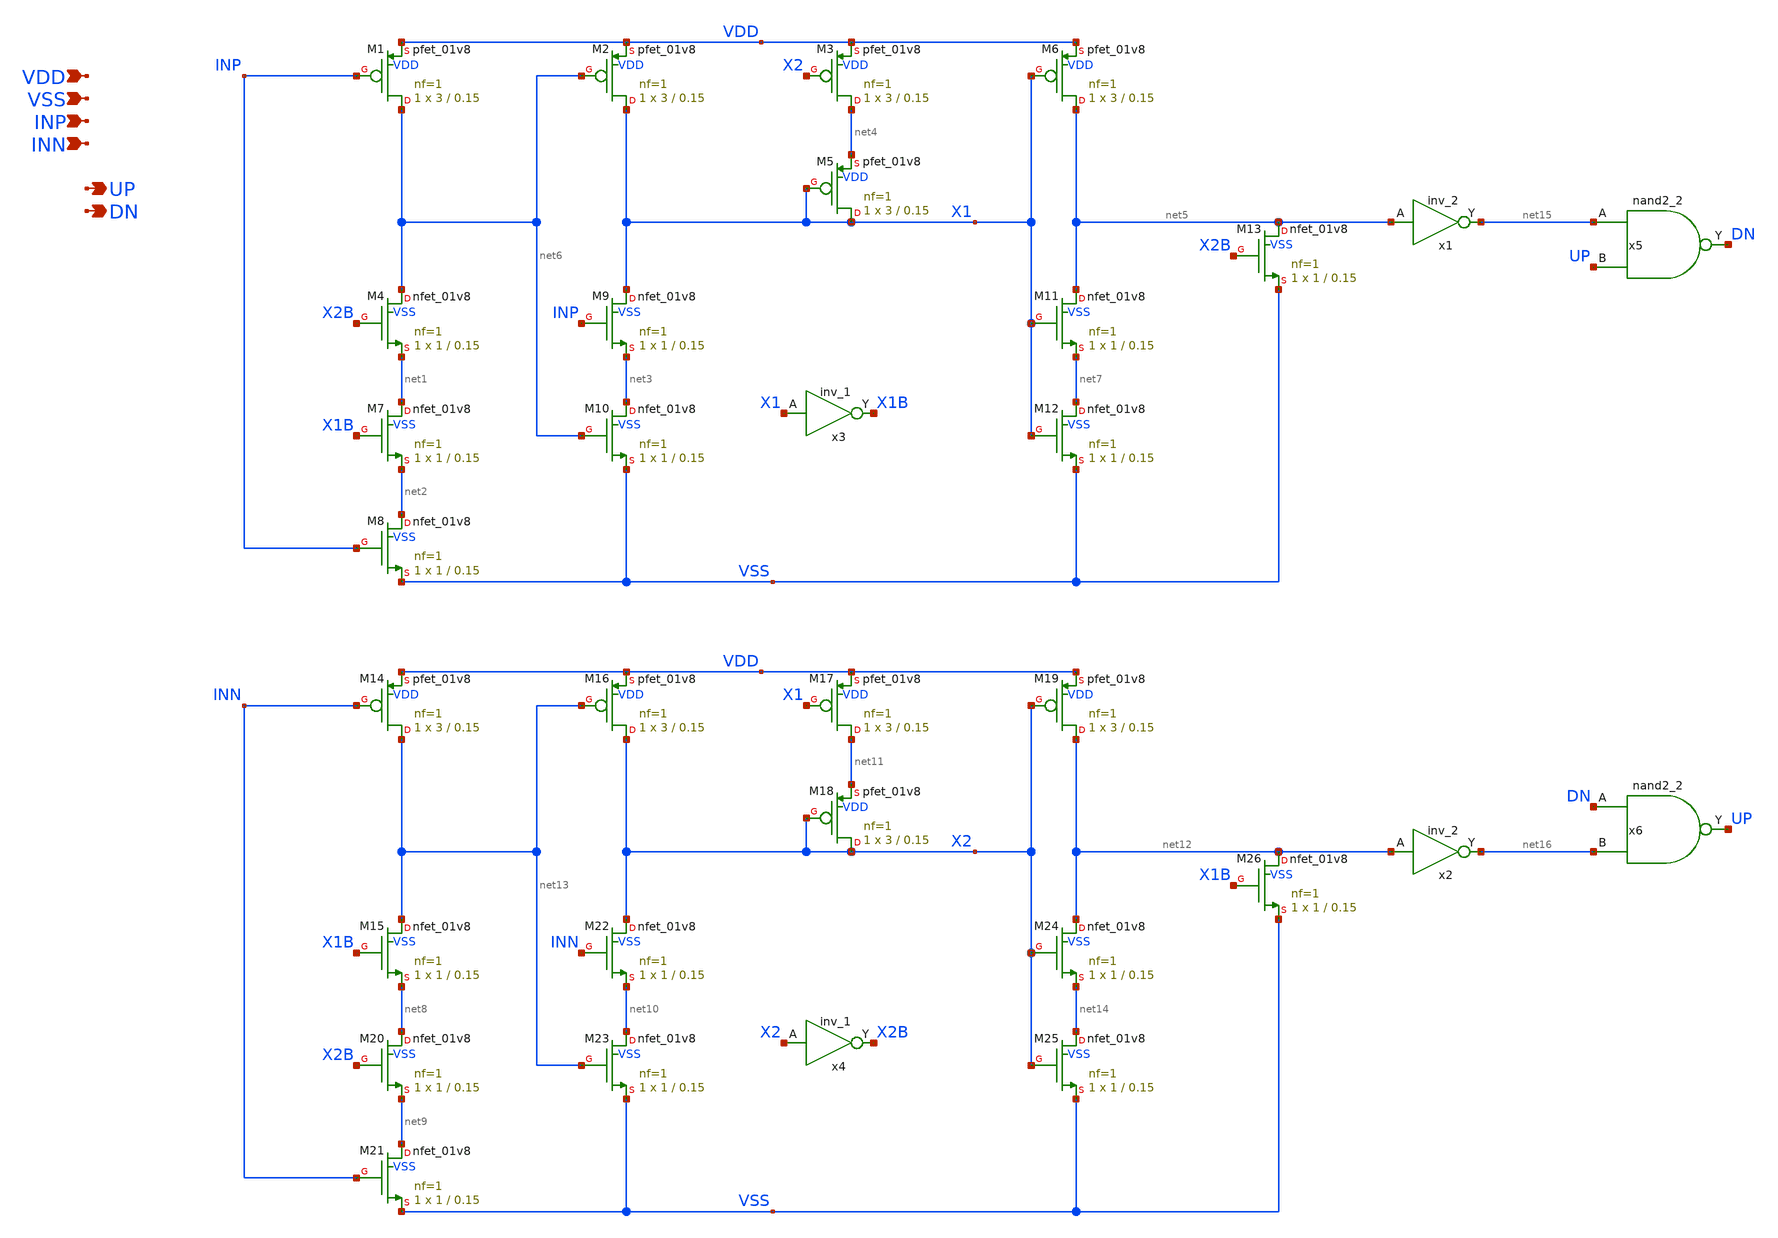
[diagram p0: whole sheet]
** sch_path: xschem/pfd.sch
**.subckt pfd VDD VSS INP INN UP DN
*.ipin VDD
*.ipin VSS
*.ipin INP
*.ipin INN
*.opin UP
*.opin DN
XM1 net6 INP VDD VDD sky130_fd_pr__pfet_01v8 L=0.15 W=3 nf=1 ad='int((nf+1)/2) * W/nf * 0.29' as='int((nf+2)/2) * W/nf * 0.29'
+ pd='2*int((nf+1)/2) * (W/nf + 0.29)' ps='2*int((nf+2)/2) * (W/nf + 0.29)' nrd='0.29 / W' nrs='0.29 / W'
+ sa=0 sb=0 sd=0 mult=1 m=1
XM4 net6 X2B net1 VSS sky130_fd_pr__nfet_01v8 L=0.15 W=1 nf=1 ad='int((nf+1)/2) * W/nf * 0.29' as='int((nf+2)/2) * W/nf * 0.29'
+ pd='2*int((nf+1)/2) * (W/nf + 0.29)' ps='2*int((nf+2)/2) * (W/nf + 0.29)' nrd='0.29 / W' nrs='0.29 / W'
+ sa=0 sb=0 sd=0 mult=1 m=1
XM2 X1 net6 VDD VDD sky130_fd_pr__pfet_01v8 L=0.15 W=3 nf=1 ad='int((nf+1)/2) * W/nf * 0.29' as='int((nf+2)/2) * W/nf * 0.29'
+ pd='2*int((nf+1)/2) * (W/nf + 0.29)' ps='2*int((nf+2)/2) * (W/nf + 0.29)' nrd='0.29 / W' nrs='0.29 / W'
+ sa=0 sb=0 sd=0 mult=1 m=1
XM3 net4 X2 VDD VDD sky130_fd_pr__pfet_01v8 L=0.15 W=3 nf=1 ad='int((nf+1)/2) * W/nf * 0.29' as='int((nf+2)/2) * W/nf * 0.29'
+ pd='2*int((nf+1)/2) * (W/nf + 0.29)' ps='2*int((nf+2)/2) * (W/nf + 0.29)' nrd='0.29 / W' nrs='0.29 / W'
+ sa=0 sb=0 sd=0 mult=1 m=1
XM5 X1 X1 net4 VDD sky130_fd_pr__pfet_01v8 L=0.15 W=3 nf=1 ad='int((nf+1)/2) * W/nf * 0.29' as='int((nf+2)/2) * W/nf * 0.29'
+ pd='2*int((nf+1)/2) * (W/nf + 0.29)' ps='2*int((nf+2)/2) * (W/nf + 0.29)' nrd='0.29 / W' nrs='0.29 / W'
+ sa=0 sb=0 sd=0 mult=1 m=1
XM6 net5 X1 VDD VDD sky130_fd_pr__pfet_01v8 L=0.15 W=3 nf=1 ad='int((nf+1)/2) * W/nf * 0.29' as='int((nf+2)/2) * W/nf * 0.29'
+ pd='2*int((nf+1)/2) * (W/nf + 0.29)' ps='2*int((nf+2)/2) * (W/nf + 0.29)' nrd='0.29 / W' nrs='0.29 / W'
+ sa=0 sb=0 sd=0 mult=1 m=1
XM7 net1 X1B net2 VSS sky130_fd_pr__nfet_01v8 L=0.15 W=1 nf=1 ad='int((nf+1)/2) * W/nf * 0.29' as='int((nf+2)/2) * W/nf * 0.29'
+ pd='2*int((nf+1)/2) * (W/nf + 0.29)' ps='2*int((nf+2)/2) * (W/nf + 0.29)' nrd='0.29 / W' nrs='0.29 / W'
+ sa=0 sb=0 sd=0 mult=1 m=1
XM8 net2 INP VSS VSS sky130_fd_pr__nfet_01v8 L=0.15 W=1 nf=1 ad='int((nf+1)/2) * W/nf * 0.29' as='int((nf+2)/2) * W/nf * 0.29'
+ pd='2*int((nf+1)/2) * (W/nf + 0.29)' ps='2*int((nf+2)/2) * (W/nf + 0.29)' nrd='0.29 / W' nrs='0.29 / W'
+ sa=0 sb=0 sd=0 mult=1 m=1
XM9 X1 INP net3 VSS sky130_fd_pr__nfet_01v8 L=0.15 W=1 nf=1 ad='int((nf+1)/2) * W/nf * 0.29' as='int((nf+2)/2) * W/nf * 0.29'
+ pd='2*int((nf+1)/2) * (W/nf + 0.29)' ps='2*int((nf+2)/2) * (W/nf + 0.29)' nrd='0.29 / W' nrs='0.29 / W'
+ sa=0 sb=0 sd=0 mult=1 m=1
XM10 net3 net6 VSS VSS sky130_fd_pr__nfet_01v8 L=0.15 W=1 nf=1 ad='int((nf+1)/2) * W/nf * 0.29' as='int((nf+2)/2) * W/nf * 0.29'
+ pd='2*int((nf+1)/2) * (W/nf + 0.29)' ps='2*int((nf+2)/2) * (W/nf + 0.29)' nrd='0.29 / W' nrs='0.29 / W'
+ sa=0 sb=0 sd=0 mult=1 m=1
XM11 net5 X1 net7 VSS sky130_fd_pr__nfet_01v8 L=0.15 W=1 nf=1 ad='int((nf+1)/2) * W/nf * 0.29' as='int((nf+2)/2) * W/nf * 0.29'
+ pd='2*int((nf+1)/2) * (W/nf + 0.29)' ps='2*int((nf+2)/2) * (W/nf + 0.29)' nrd='0.29 / W' nrs='0.29 / W'
+ sa=0 sb=0 sd=0 mult=1 m=1
XM12 net7 X1 VSS VSS sky130_fd_pr__nfet_01v8 L=0.15 W=1 nf=1 ad='int((nf+1)/2) * W/nf * 0.29' as='int((nf+2)/2) * W/nf * 0.29'
+ pd='2*int((nf+1)/2) * (W/nf + 0.29)' ps='2*int((nf+2)/2) * (W/nf + 0.29)' nrd='0.29 / W' nrs='0.29 / W'
+ sa=0 sb=0 sd=0 mult=1 m=1
XM13 net5 X2B VSS VSS sky130_fd_pr__nfet_01v8 L=0.15 W=1 nf=1 ad='int((nf+1)/2) * W/nf * 0.29' as='int((nf+2)/2) * W/nf * 0.29'
+ pd='2*int((nf+1)/2) * (W/nf + 0.29)' ps='2*int((nf+2)/2) * (W/nf + 0.29)' nrd='0.29 / W' nrs='0.29 / W'
+ sa=0 sb=0 sd=0 mult=1 m=1
XM14 net13 INN VDD VDD sky130_fd_pr__pfet_01v8 L=0.15 W=3 nf=1 ad='int((nf+1)/2) * W/nf * 0.29' as='int((nf+2)/2) * W/nf * 0.29'
+ pd='2*int((nf+1)/2) * (W/nf + 0.29)' ps='2*int((nf+2)/2) * (W/nf + 0.29)' nrd='0.29 / W' nrs='0.29 / W'
+ sa=0 sb=0 sd=0 mult=1 m=1
XM15 net13 X1B net8 VSS sky130_fd_pr__nfet_01v8 L=0.15 W=1 nf=1 ad='int((nf+1)/2) * W/nf * 0.29' as='int((nf+2)/2) * W/nf * 0.29'
+ pd='2*int((nf+1)/2) * (W/nf + 0.29)' ps='2*int((nf+2)/2) * (W/nf + 0.29)' nrd='0.29 / W' nrs='0.29 / W'
+ sa=0 sb=0 sd=0 mult=1 m=1
XM16 X2 net13 VDD VDD sky130_fd_pr__pfet_01v8 L=0.15 W=3 nf=1 ad='int((nf+1)/2) * W/nf * 0.29' as='int((nf+2)/2) * W/nf * 0.29'
+ pd='2*int((nf+1)/2) * (W/nf + 0.29)' ps='2*int((nf+2)/2) * (W/nf + 0.29)' nrd='0.29 / W' nrs='0.29 / W'
+ sa=0 sb=0 sd=0 mult=1 m=1
XM17 net11 X1 VDD VDD sky130_fd_pr__pfet_01v8 L=0.15 W=3 nf=1 ad='int((nf+1)/2) * W/nf * 0.29' as='int((nf+2)/2) * W/nf * 0.29'
+ pd='2*int((nf+1)/2) * (W/nf + 0.29)' ps='2*int((nf+2)/2) * (W/nf + 0.29)' nrd='0.29 / W' nrs='0.29 / W'
+ sa=0 sb=0 sd=0 mult=1 m=1
XM18 X2 X2 net11 VDD sky130_fd_pr__pfet_01v8 L=0.15 W=3 nf=1 ad='int((nf+1)/2) * W/nf * 0.29' as='int((nf+2)/2) * W/nf * 0.29'
+ pd='2*int((nf+1)/2) * (W/nf + 0.29)' ps='2*int((nf+2)/2) * (W/nf + 0.29)' nrd='0.29 / W' nrs='0.29 / W'
+ sa=0 sb=0 sd=0 mult=1 m=1
XM19 net12 X2 VDD VDD sky130_fd_pr__pfet_01v8 L=0.15 W=3 nf=1 ad='int((nf+1)/2) * W/nf * 0.29' as='int((nf+2)/2) * W/nf * 0.29'
+ pd='2*int((nf+1)/2) * (W/nf + 0.29)' ps='2*int((nf+2)/2) * (W/nf + 0.29)' nrd='0.29 / W' nrs='0.29 / W'
+ sa=0 sb=0 sd=0 mult=1 m=1
XM20 net8 X2B net9 VSS sky130_fd_pr__nfet_01v8 L=0.15 W=1 nf=1 ad='int((nf+1)/2) * W/nf * 0.29' as='int((nf+2)/2) * W/nf * 0.29'
+ pd='2*int((nf+1)/2) * (W/nf + 0.29)' ps='2*int((nf+2)/2) * (W/nf + 0.29)' nrd='0.29 / W' nrs='0.29 / W'
+ sa=0 sb=0 sd=0 mult=1 m=1
XM21 net9 INN VSS VSS sky130_fd_pr__nfet_01v8 L=0.15 W=1 nf=1 ad='int((nf+1)/2) * W/nf * 0.29' as='int((nf+2)/2) * W/nf * 0.29'
+ pd='2*int((nf+1)/2) * (W/nf + 0.29)' ps='2*int((nf+2)/2) * (W/nf + 0.29)' nrd='0.29 / W' nrs='0.29 / W'
+ sa=0 sb=0 sd=0 mult=1 m=1
XM22 X2 INN net10 VSS sky130_fd_pr__nfet_01v8 L=0.15 W=1 nf=1 ad='int((nf+1)/2) * W/nf * 0.29' as='int((nf+2)/2) * W/nf * 0.29'
+ pd='2*int((nf+1)/2) * (W/nf + 0.29)' ps='2*int((nf+2)/2) * (W/nf + 0.29)' nrd='0.29 / W' nrs='0.29 / W'
+ sa=0 sb=0 sd=0 mult=1 m=1
XM23 net10 net13 VSS VSS sky130_fd_pr__nfet_01v8 L=0.15 W=1 nf=1 ad='int((nf+1)/2) * W/nf * 0.29' as='int((nf+2)/2) * W/nf * 0.29'
+ pd='2*int((nf+1)/2) * (W/nf + 0.29)' ps='2*int((nf+2)/2) * (W/nf + 0.29)' nrd='0.29 / W' nrs='0.29 / W'
+ sa=0 sb=0 sd=0 mult=1 m=1
XM24 net12 X2 net14 VSS sky130_fd_pr__nfet_01v8 L=0.15 W=1 nf=1 ad='int((nf+1)/2) * W/nf * 0.29' as='int((nf+2)/2) * W/nf * 0.29'
+ pd='2*int((nf+1)/2) * (W/nf + 0.29)' ps='2*int((nf+2)/2) * (W/nf + 0.29)' nrd='0.29 / W' nrs='0.29 / W'
+ sa=0 sb=0 sd=0 mult=1 m=1
XM25 net14 X2 VSS VSS sky130_fd_pr__nfet_01v8 L=0.15 W=1 nf=1 ad='int((nf+1)/2) * W/nf * 0.29' as='int((nf+2)/2) * W/nf * 0.29'
+ pd='2*int((nf+1)/2) * (W/nf + 0.29)' ps='2*int((nf+2)/2) * (W/nf + 0.29)' nrd='0.29 / W' nrs='0.29 / W'
+ sa=0 sb=0 sd=0 mult=1 m=1
XM26 net12 X1B VSS VSS sky130_fd_pr__nfet_01v8 L=0.15 W=1 nf=1 ad='int((nf+1)/2) * W/nf * 0.29' as='int((nf+2)/2) * W/nf * 0.29'
+ pd='2*int((nf+1)/2) * (W/nf + 0.29)' ps='2*int((nf+2)/2) * (W/nf + 0.29)' nrd='0.29 / W' nrs='0.29 / W'
+ sa=0 sb=0 sd=0 mult=1 m=1
x3 X1 VSS VSS VDD VDD X1B sky130_fd_sc_hd__inv_1
x4 X2 VSS VSS VDD VDD X2B sky130_fd_sc_hd__inv_1
x1 net5 VSS VSS VDD VDD net15 sky130_fd_sc_hd__inv_2
x2 net12 VSS VSS VDD VDD net16 sky130_fd_sc_hd__inv_2
x5 net15 UP VSS VSS VDD VDD DN sky130_fd_sc_hd__nand2_2
x6 DN net16 VSS VSS VDD VDD UP sky130_fd_sc_hd__nand2_2
**.ends
.end
